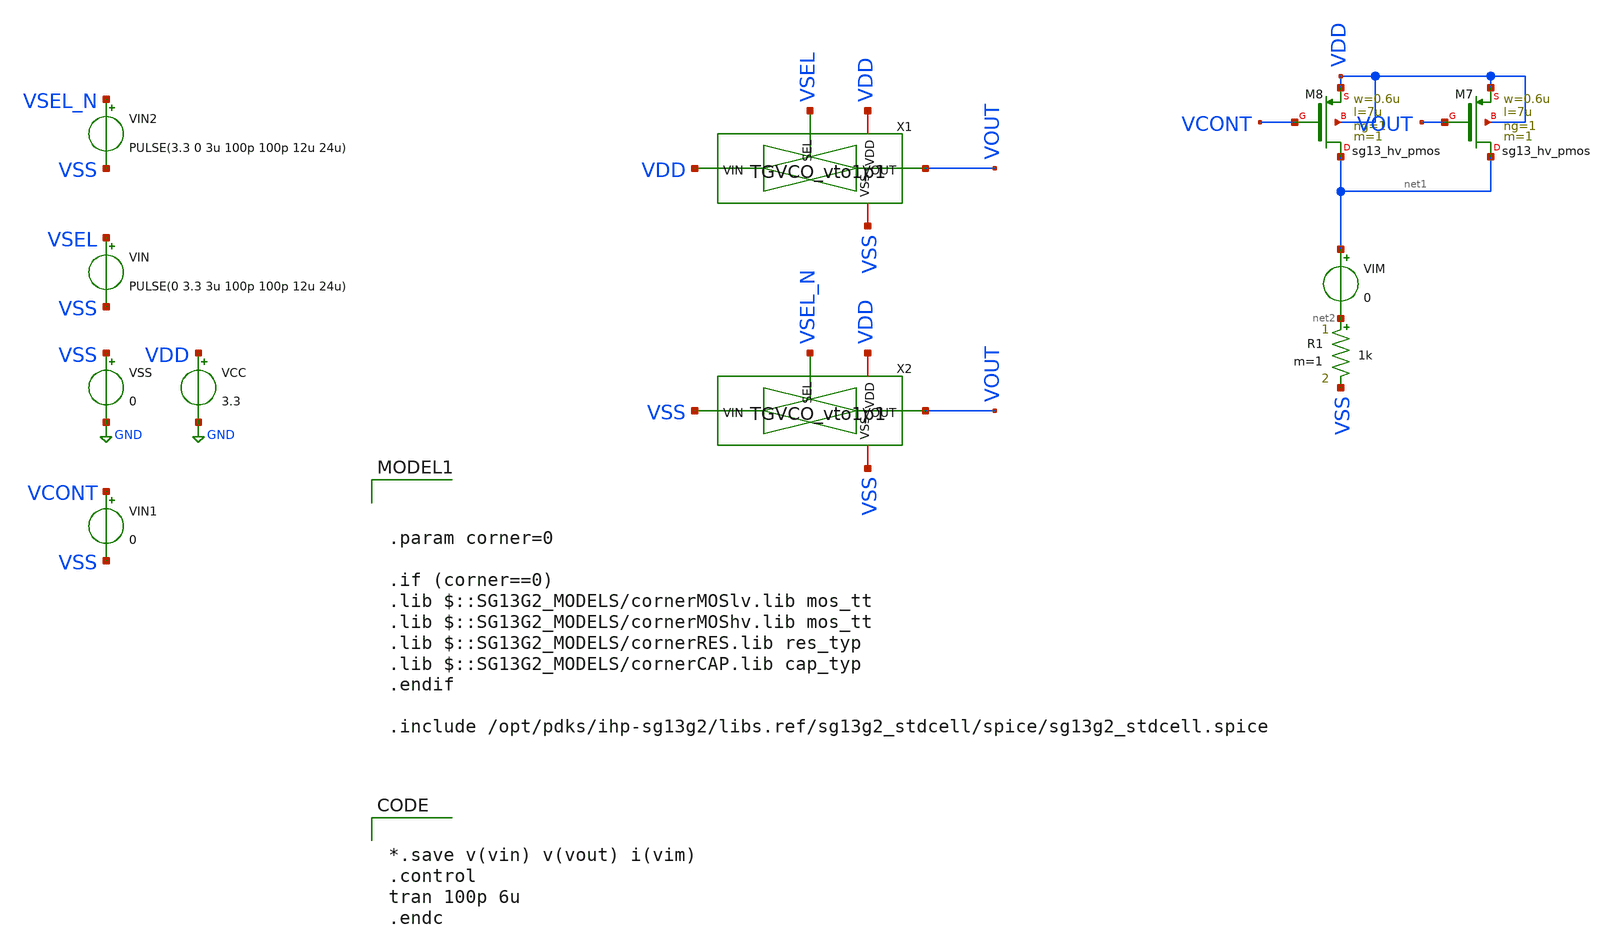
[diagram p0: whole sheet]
** sch_path: ChipUSM_AnalogTrack24/LSLH/tb_TGVCO_vto1p1.sch
**.subckt tb_TGVCO_vto1p1
VCC VDD GND 3.3
VSS VSS GND 0
VIN VSEL VSS PULSE(0 3.3 3u 100p 100p 12u 24u)
X1 VDD VSEL VOUT VDD VSS TGVCO_vto1p1
VIN1 VCONT VSS 0
VIN2 VSEL_N VSS PULSE(3.3 0 3u 100p 100p 12u 24u)
XM8 net1 VCONT VDD VDD sg13_hv_pmos w=0.6u l=7u ng=1 m=1 mm_ok=1
XM7 net1 VOUT VDD VDD sg13_hv_pmos w=0.6u l=7u ng=1 m=1 mm_ok=1
R1 net2 VSS 1k m=1
VIM net1 net2 0
X2 VDD VSEL_N VOUT VSS VSS TGVCO_vto1p1
**** begin user architecture code


*.save v(vin) v(vout) i(vim)
.control
tran 100p 6u
.endc




.param corner=0

.if (corner==0)
.lib $::SG13G2_MODELS/cornerMOSlv.lib mos_tt
.lib $::SG13G2_MODELS/cornerMOShv.lib mos_tt
.lib $::SG13G2_MODELS/cornerRES.lib res_typ
.lib $::SG13G2_MODELS/cornerCAP.lib cap_typ
.endif

.include /opt/pdks/ihp-sg13g2/libs.ref/sg13g2_stdcell/spice/sg13g2_stdcell.spice

**** end user architecture code
**.ends

* expanding   symbol:  TGVCO_vto1p1.sym # of pins=5
** sym_path: ChipUSM_AnalogTrack24/LSLH/TGVCO_vto1p1.sym
** sch_path: ChipUSM_AnalogTrack24/LSLH/TGVCO_vto1p1.sch
.subckt TGVCO_vto1p1 VDD SEL VOUT VIN VSS
*.iopin VDD
*.ipin SEL
*.opin VOUT
*.iopin VSS
*.ipin VIN
XMD5 SEL_N SEL VDD VDD sg13_hv_pmos w=1u l=0.5u ng=1 m=2 mm_ok=1
XMD6 VSS SEL SEL_N VSS sg13_hv_nmos w=1u l=0.5u ng=1 m=1 mm_ok=1
XMD1 VIN SEL VOUT VSS sg13_hv_nmos w=1u l=0.5u ng=1 m=1 mm_ok=1
XMD2 VIN SEL_N VOUT VDD sg13_hv_pmos w=1u l=0.5u ng=1 m=2 mm_ok=1
.ends

.GLOBAL GND
.end
